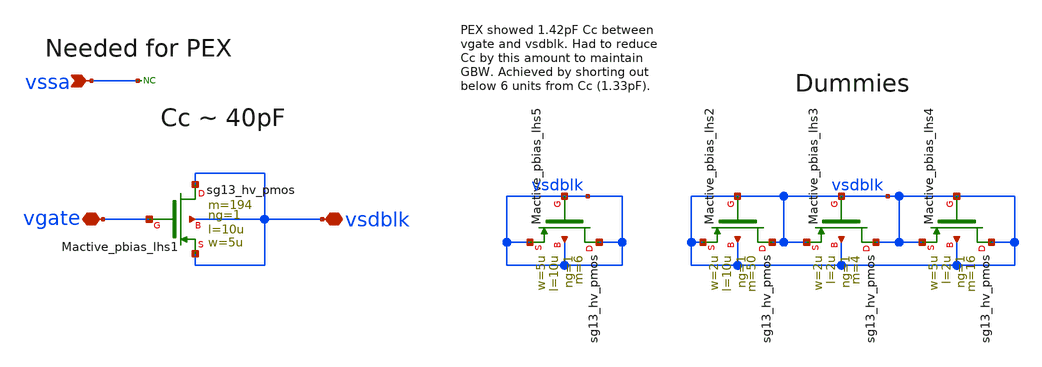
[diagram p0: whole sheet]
** sch_path: Schematics_Layout/sunrise_opamp_Cc/sunrise_opamp_Cc.sch
* Cc by this amount to maintain
**.subckt sunrise_opamp_Cc vsdblk vgate vssa
*.iopin vsdblk
*.iopin vgate
*.ipin vssa
XMactive_pbias_lhs1 vsdblk vgate vsdblk vsdblk sg13_hv_pmos w=5u l=10u ng=1 m=194 mm_ok=1
XMactive_pbias_lhs2 vsdblk vsdblk vsdblk vsdblk sg13_hv_pmos w=2u l=10u ng=1 m=50 mm_ok=1
XMactive_pbias_lhs3 vsdblk vsdblk vsdblk vsdblk sg13_hv_pmos w=2u l=2u ng=1 m=4 mm_ok=1
XMactive_pbias_lhs4 vsdblk vsdblk vsdblk vsdblk sg13_hv_pmos w=5u l=2u ng=1 m=16 mm_ok=1
* noconn vssa
XMactive_pbias_lhs5 vsdblk vsdblk vsdblk vsdblk sg13_hv_pmos w=5u l=10u ng=1 m=6 mm_ok=1
**.ends
.end
